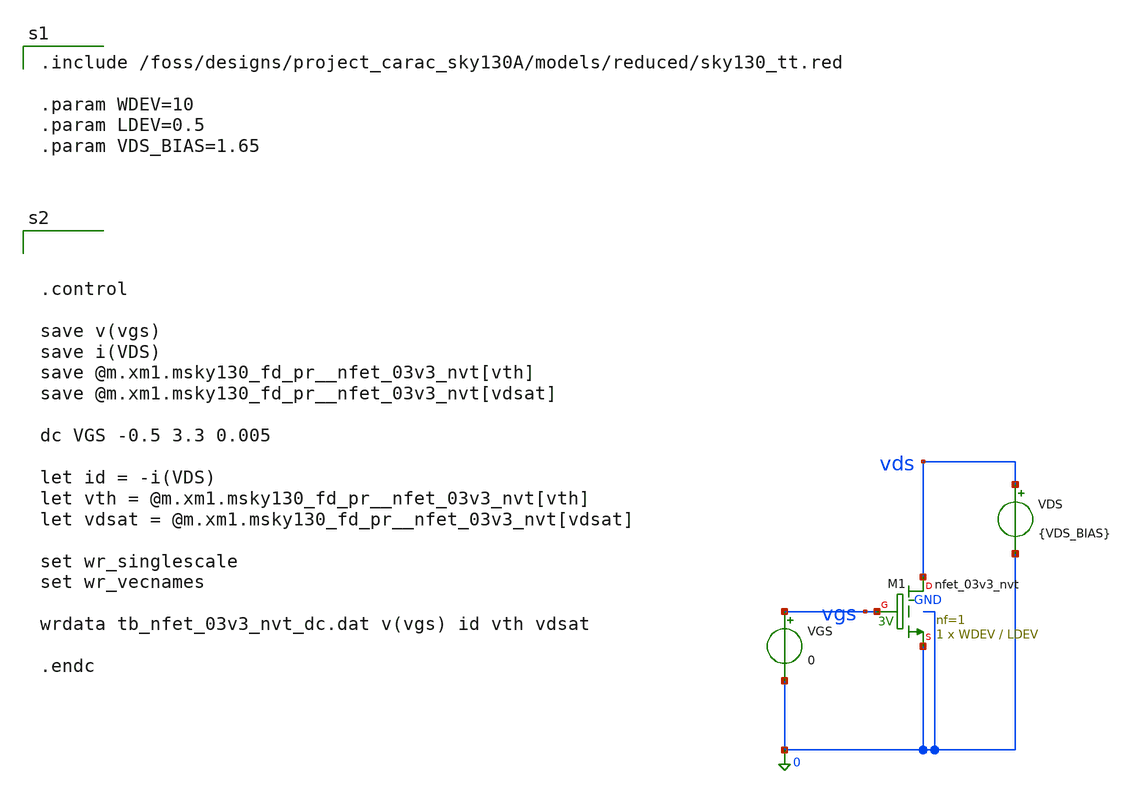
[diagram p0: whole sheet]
** sch_path: dfii/project_carac_sky130A_sim/tb_nfet_03v3_nvt_dc.sch
* Copyright 2021 Stefan Frederik Schippers
* Licensed under the Apache License, Version 2.0 (the "License");
* you may not use this file except in compliance with the License.
* You may obtain a copy of the License at
* https://www.apache.org/licenses/LICENSE-2.0
* Unless required by applicable law or agreed to in writing, software
* distributed under the License is distributed on an "AS IS" BASIS,
* WITHOUT WARRANTIES OR CONDITIONS OF ANY KIND, either express or implied.
* See the License for the specific language governing permissions and
* limitations under the License.

.include /foss/designs/project_carac_sky130A/models/reduced/sky130_tt.red

.param WDEV=10
.param LDEV=0.5
.param VDS_BIAS=1.65



**.subckt tb_nfet_03v3_nvt_dc
XM1 vds vgs 0 GND sky130_fd_pr__nfet_03v3_nvt L=LDEV W=WDEV nf=1 ad='int((1 + 1)/2) * WDEV / 1 * 0.29'
+ as='int((1 + 2)/2) * WDEV / 1 * 0.29' pd='2*int((1 + 1)/2) * (WDEV / 1 + 0.29)' ps='2*int((1 + 2)/2) * (WDEV / 1 + 0.29)'
+ nrd='0.29 / WDEV ' nrs='0.29 / WDEV ' sa=0 sb=0 sd=0 mult=1 m=1
VGS vgs 0 0
VDS vds 0 {VDS_BIAS}
**.ends
**** begin user architecture code



.control

save v(vgs)
save i(VDS)
save @m.xm1.msky130_fd_pr__nfet_03v3_nvt[vth]
save @m.xm1.msky130_fd_pr__nfet_03v3_nvt[vdsat]

dc VGS -0.5 3.3 0.005

let id = -i(VDS)
let vth = @m.xm1.msky130_fd_pr__nfet_03v3_nvt[vth]
let vdsat = @m.xm1.msky130_fd_pr__nfet_03v3_nvt[vdsat]

set wr_singlescale
set wr_vecnames

wrdata tb_nfet_03v3_nvt_dc.dat v(vgs) id vth vdsat

.endc

**** end user architecture code
.end
